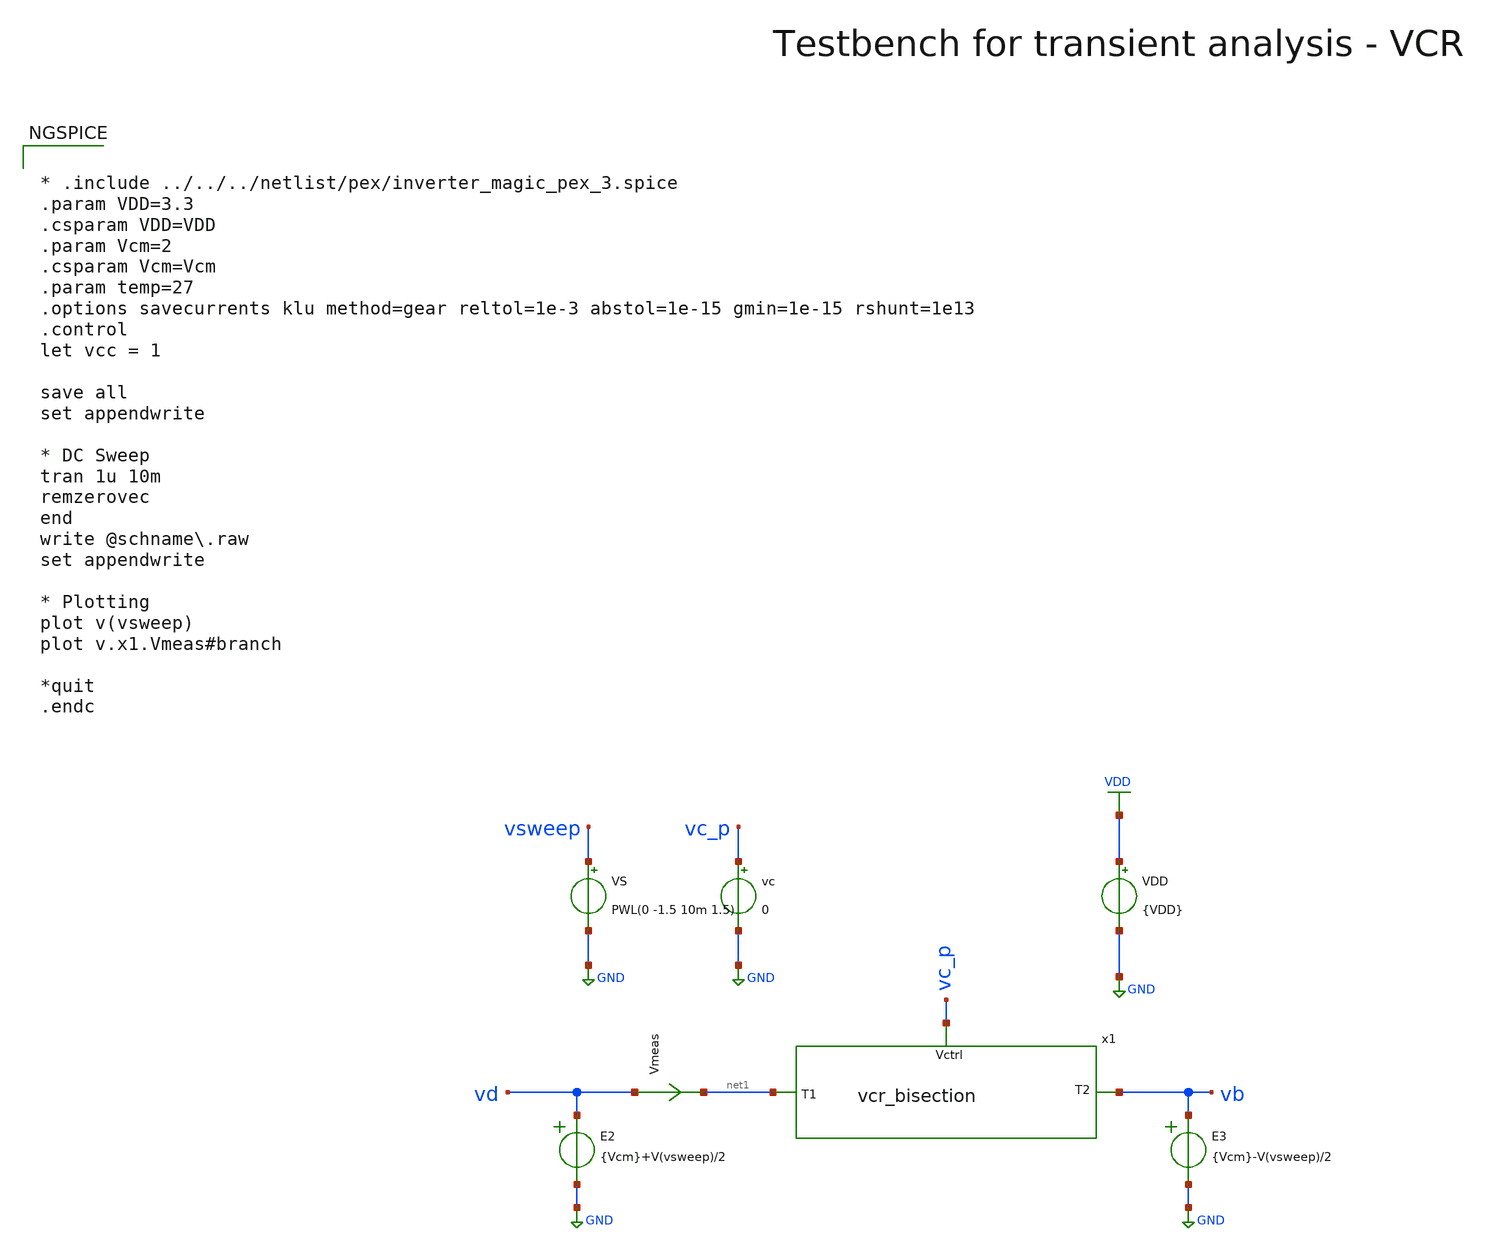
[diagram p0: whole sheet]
** sch_path: macros/voltage_controlled_resistors/macros/vcr_bisection/testbenches/xschem/res_tb_tran.sch
**.subckt res_tb_tran
VDD VDD GND {VDD}
VS vsweep GND PWL(0 -1.5 10m 1.5)
Vmeas vd net1 0
.save i(vmeas)
E2 vd GND VOL=' {Vcm}+V(vsweep)/2 '
E3 vb GND VOL=' {Vcm}-V(vsweep)/2 '
vc vc_p GND 0
x1 vc_p net1 vb vcr_bisection
**** begin user architecture code

.lib cornerMOSlv.lib mos_tt
.lib cornerMOShv.lib mos_tt
.lib cornerRES.lib res_typ
.lib cornerDIO.lib dio_tt



* .include ../../../netlist/pex/inverter_magic_pex_3.spice
.param VDD=3.3
.csparam VDD=VDD
.param Vcm=2
.csparam Vcm=Vcm
.param temp=27
.options savecurrents klu method=gear reltol=1e-3 abstol=1e-15 gmin=1e-15 rshunt=1e13
.control
let vcc = 1

save all
set appendwrite

* DC Sweep
tran 1u 10m
remzerovec
end
write @schname\.raw
set appendwrite

* Plotting
plot v(vsweep)
plot v.x1.Vmeas#branch

*quit
.endc


**** end user architecture code
**.ends

* expanding   symbol:  vcr_bisection.sym # of pins=3
** sym_path: macros/heichips26_analog_project/macros/vcr_bisection/schematic/xschem/vcr_bisection.sym
** sch_path: macros/heichips26_analog_project/macros/vcr_bisection/schematic/xschem/vcr_bisection.sch
.subckt vcr_bisection Vctrl T1 T2
*.ipin T1
*.ipin T2
*.ipin Vctrl
R1 vcm T1 10k m=1
R2 T2 vcm 10k m=1
Vmeas T1 net1 0
.save i(vmeas)
XM1 net1 Vctrl T2 vcm sg13_hv_pmos w=50u l=10u ng=10 m=1 mm_ok=1
.ends

.GLOBAL GND
.GLOBAL VDD
.end
